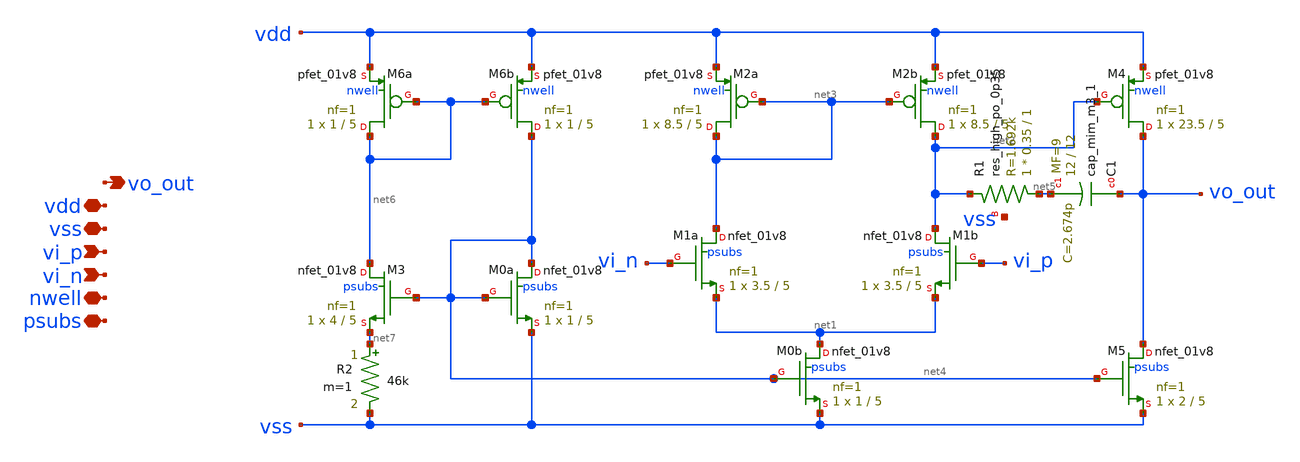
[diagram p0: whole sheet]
** sch_path: xschem/op.sch
**.subckt op vss vdd vo_out vi_p vi_n psubs nwell
*.iopin vss
*.iopin vdd
*.opin vo_out
*.ipin vi_p
*.ipin vi_n
*.iopin psubs
*.iopin nwell
XM1a net3 vi_n net1 psubs sky130_fd_pr__nfet_01v8 L=5 W=3.5 nf=1 ad='int((nf+1)/2) * W/nf * 0.29' as='int((nf+2)/2) * W/nf * 0.29'
+ pd='2*int((nf+1)/2) * (W/nf + 0.29)' ps='2*int((nf+2)/2) * (W/nf + 0.29)' nrd='0.29 / W' nrs='0.29 / W'
+ sa=0 sb=0 sd=0 mult=1 m=1
XM2a net3 net3 vdd nwell sky130_fd_pr__pfet_01v8 L=5 W=8.5 nf=1 ad='int((1 + 1)/2) * 8.5 / 1 * 0.29'
+ as='int((1 + 2)/2) * 8.5 / 1 * 0.29' pd='2*int((1 + 1)/2) * (8.5 / 1 + 0.29)' ps='2*int((1 + 2)/2) * (8.5 / 1 + 0.29)'
+ nrd='0.29 / 8.5 ' nrs='0.29 / 8.5 ' sa=0 sb=0 sd=0 mult=1 m=1
XM0a net4 net4 vss psubs sky130_fd_pr__nfet_01v8 L=5 W=1 nf=1 ad='int((1 + 1)/2) * 1 / 1 * 0.29' as='int((1 + 2)/2) * 1 / 1 * 0.29'
+ pd='2*int((1 + 1)/2) * (1 / 1 + 0.29)' ps='2*int((1 + 2)/2) * (1 / 1 + 0.29)' nrd='0.29 / 1 ' nrs='0.29 / 1 '
+ sa=0 sb=0 sd=0 mult=1 m=1
XM0b net1 net4 vss psubs sky130_fd_pr__nfet_01v8 L=5 W=1 nf=1 ad='int((1 + 1)/2) * 1 / 1 * 0.29' as='int((1 + 2)/2) * 1 / 1 * 0.29'
+ pd='2*int((1 + 1)/2) * (1 / 1 + 0.29)' ps='2*int((1 + 2)/2) * (1 / 1 + 0.29)' nrd='0.29 / 1 ' nrs='0.29 / 1 '
+ sa=0 sb=0 sd=0 mult=1 m=1
XM4 vo_out net2 vdd nwell sky130_fd_pr__pfet_01v8 L=5 W=23.5 nf=1 ad='int((1 + 1)/2) * 23.5 / 1 * 0.29'
+ as='int((1 + 2)/2) * 23.5 / 1 * 0.29' pd='2*int((1 + 1)/2) * (23.5 / 1 + 0.29)' ps='2*int((1 + 2)/2) * (23.5 / 1 + 0.29)'
+ nrd='0.29 / 23.5 ' nrs='0.29 / 23.5 ' sa=0 sb=0 sd=0 mult=1 m=1
XM5 vo_out net4 vss psubs sky130_fd_pr__nfet_01v8 L=5 W=2 nf=1 ad='int((1 + 1)/2) * 2 / 1 * 0.29' as='int((1 + 2)/2) * 2 / 1 * 0.29'
+ pd='2*int((1 + 1)/2) * (2 / 1 + 0.29)' ps='2*int((1 + 2)/2) * (2 / 1 + 0.29)' nrd='0.29 / 2 ' nrs='0.29 / 2 '
+ sa=0 sb=0 sd=0 mult=1 m=1
XM1b net2 vi_p net1 psubs sky130_fd_pr__nfet_01v8 L=5 W=3.5 nf=1 ad='int((nf+1)/2) * W/nf * 0.29' as='int((nf+2)/2) * W/nf * 0.29'
+ pd='2*int((nf+1)/2) * (W/nf + 0.29)' ps='2*int((nf+2)/2) * (W/nf + 0.29)' nrd='0.29 / W' nrs='0.29 / W'
+ sa=0 sb=0 sd=0 mult=1 m=1
XM2b net2 net3 vdd nwell sky130_fd_pr__pfet_01v8 L=5 W=8.5 nf=1 ad='int((1 + 1)/2) * 8.5 / 1 * 0.29'
+ as='int((1 + 2)/2) * 8.5 / 1 * 0.29' pd='2*int((1 + 1)/2) * (8.5 / 1 + 0.29)' ps='2*int((1 + 2)/2) * (8.5 / 1 + 0.29)'
+ nrd='0.29 / 8.5 ' nrs='0.29 / 8.5 ' sa=0 sb=0 sd=0 mult=1 m=1
XC1 vo_out net5 sky130_fd_pr__cap_mim_m3_1 W=12 L=12 MF=9 m=9
XM3 net6 net4 net7 psubs sky130_fd_pr__nfet_01v8 L=5 W=4 nf=1 ad='int((1 + 1)/2) * 4 / 1 * 0.29' as='int((1 + 2)/2) * 4 / 1 * 0.29'
+ pd='2*int((1 + 1)/2) * (4 / 1 + 0.29)' ps='2*int((1 + 2)/2) * (4 / 1 + 0.29)' nrd='0.29 / 4 ' nrs='0.29 / 4 '
+ sa=0 sb=0 sd=0 mult=1 m=1
XM6a net6 net6 vdd nwell sky130_fd_pr__pfet_01v8 L=5 W=1 nf=1 ad='int((1 + 1)/2) * 1 / 1 * 0.29' as='int((1 + 2)/2) * 1 / 1 * 0.29'
+ pd='2*int((1 + 1)/2) * (1 / 1 + 0.29)' ps='2*int((1 + 2)/2) * (1 / 1 + 0.29)' nrd='0.29 / 1 ' nrs='0.29 / 1 '
+ sa=0 sb=0 sd=0 mult=1 m=1
XM6b net4 net6 vdd nwell sky130_fd_pr__pfet_01v8 L=5 W=1 nf=1 ad='int((1 + 1)/2) * 1 / 1 * 0.29' as='int((1 + 2)/2) * 1 / 1 * 0.29'
+ pd='2*int((1 + 1)/2) * (1 / 1 + 0.29)' ps='2*int((1 + 2)/2) * (1 / 1 + 0.29)' nrd='0.29 / 1 ' nrs='0.29 / 1 '
+ sa=0 sb=0 sd=0 mult=1 m=1
XR1 net5 net2 vss sky130_fd_pr__res_high_po_0p35 L=1 mult=1 m=1
R2 net7 vss 46k m=1
**.ends
.end
